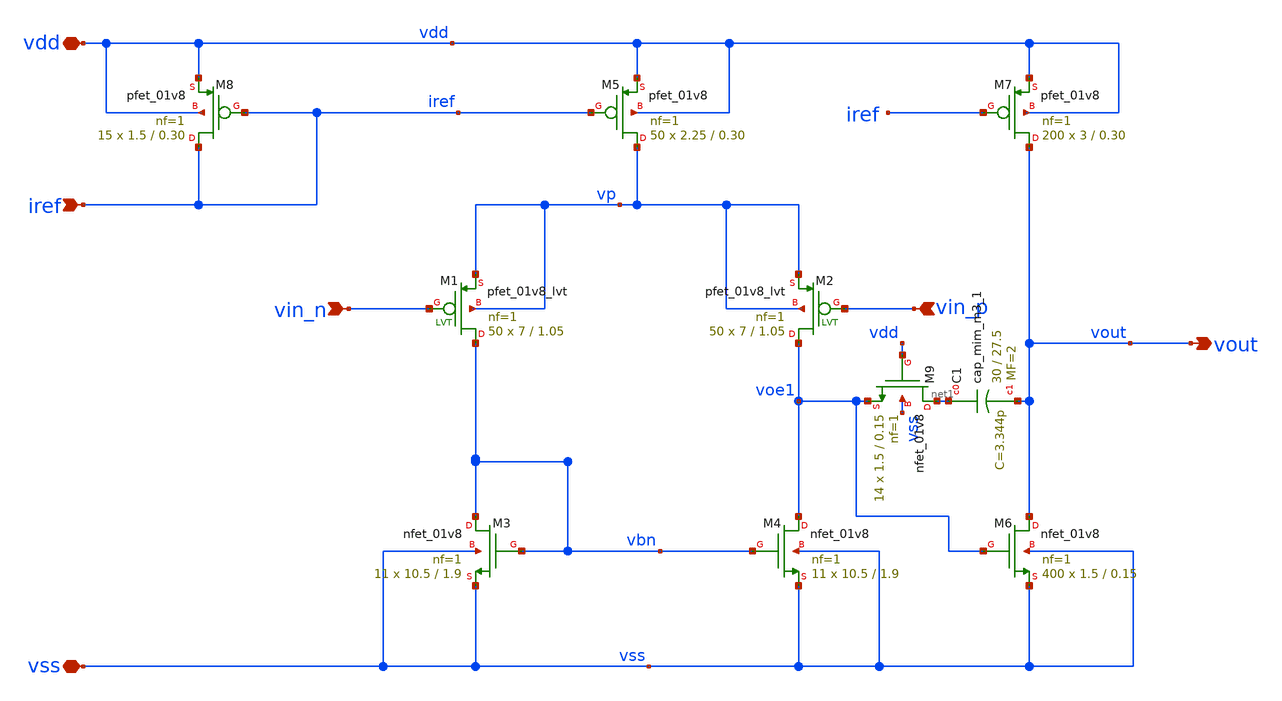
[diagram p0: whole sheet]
** sch_path: xschem/opamp_manuel.sch
**.subckt opamp_manuel vdd vss vin_n vin_p iref vout
*.iopin vdd
*.iopin vss
*.ipin vin_n
*.ipin vin_p
*.ipin iref
*.opin vout
XM3 vbn vbn vss vss sky130_fd_pr__nfet_01v8 L=1.9 W=10.5 nf=1 ad='W * 0.29' as='W * 0.29' pd='2 * (W + 0.29)'
+ ps='2 * (W + 0.29)' nrd='0.29 / W' nrs='0.29 / W' sa=0 sb=0 sd=0 mult=11 m=11
XM5 vp iref vdd vdd sky130_fd_pr__pfet_01v8 L=0.30 W=2.25 nf=1 ad='W * 0.29' as='W * 0.29' pd='2 * (W + 0.29)'
+ ps='2 * (W + 0.29)' nrd='0.29 / W' nrs='0.29 / W' sa=0 sb=0 sd=0 mult=50 m=50
XM7 vout iref vdd vdd sky130_fd_pr__pfet_01v8 L=0.30 W=3 nf=1 ad='W * 0.29' as='W * 0.29' pd='2 * (W + 0.29)'
+ ps='2 * (W + 0.29)' nrd='0.29 / W' nrs='0.29 / W' sa=0 sb=0 sd=0 mult=200 m=200
XM8 iref iref vdd vdd sky130_fd_pr__pfet_01v8 L=0.30 W=1.5 nf=1 ad='W * 0.29' as='W * 0.29' pd='2 * (W + 0.29)'
+ ps='2 * (W + 0.29)' nrd='0.29 / W' nrs='0.29 / W' sa=0 sb=0 sd=0 mult=15 m=15
XM6 vout voe1 vss vss sky130_fd_pr__nfet_01v8 L=0.15 W=1.5 nf=1 ad='W * 0.29' as='W * 0.29' pd='2 * (W + 0.29)'
+ ps='2 * (W + 0.29)' nrd='0.29 / W' nrs='0.29 / W' sa=0 sb=0 sd=0 mult=400 m=400
XM1 vbn vin_n vp vp sky130_fd_pr__pfet_01v8_lvt L=1.05 W=7 nf=1 ad='int((nf+1)/2) * W/nf * 0.29' as='int((nf+2)/2) * W/nf * 0.29'
+ pd='2*int((nf+1)/2) * (W/nf + 0.29)' ps='2*int((nf+2)/2) * (W/nf + 0.29)' nrd='0.29 / W' nrs='0.29 / W'
+ sa=0 sb=0 sd=0 mult=50 m=50
XM2 voe1 vin_p vp vp sky130_fd_pr__pfet_01v8_lvt L=1.05 W=7 nf=1 ad='int((nf+1)/2) * W/nf * 0.29' as='int((nf+2)/2) * W/nf * 0.29'
+ pd='2*int((nf+1)/2) * (W/nf + 0.29)' ps='2*int((nf+2)/2) * (W/nf + 0.29)' nrd='0.29 / W' nrs='0.29 / W'
+ sa=0 sb=0 sd=0 mult=50 m=50
XM4 voe1 vbn vss vss sky130_fd_pr__nfet_01v8 L=1.9 W=10.5 nf=1 ad='W * 0.29' as='W * 0.29' pd='2 * (W + 0.29)'
+ ps='2 * (W + 0.29)' nrd='0.29 / W' nrs='0.29 / W' sa=0 sb=0 sd=0 mult=11 m=11
XC1 net1 vout sky130_fd_pr__cap_mim_m3_1 W=30 L=27.5 MF=2 m=2
XM9 net1 vdd voe1 vss sky130_fd_pr__nfet_01v8 L=0.15 W=1.5 nf=1 ad='W * 0.29' as='W * 0.29' pd='2 * (W + 0.29)'
+ ps='2 * (W + 0.29)' nrd='0.29 / W' nrs='0.29 / W' sa=0 sb=0 sd=0 mult=14 m=14
**.ends
.end
